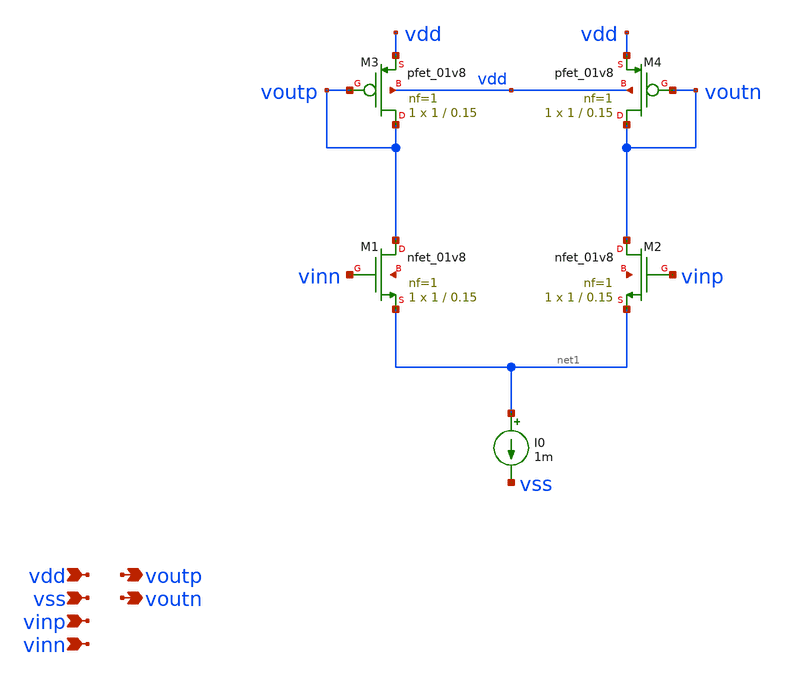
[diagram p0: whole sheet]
** sch_path: schematics/comp_pre_amp.sch
**.subckt comp_pre_amp vdd voutp vss vinp vinn voutn
*.ipin vdd
*.opin voutp
*.ipin vss
*.ipin vinp
*.ipin vinn
*.opin voutn
I0 net1 vss 1m
XM1 voutp vinn net1 net2 sky130_fd_pr__nfet_01v8 L=0.15 W=1 nf=1 ad='int((1 + 1)/2) * 1 / 1 * 0.29' as='int((1 + 2)/2) * 1 / 1 * 0.29'
+ pd='2*int((1 + 1)/2) * (1 / 1 + 0.29)' ps='2*int((1 + 2)/2) * (1 / 1 + 0.29)' nrd='0.29 / 1 ' nrs='0.29 / 1 '
+ sa=0 sb=0 sd=0 mult=1 m=1
XM2 voutn vinp net1 net3 sky130_fd_pr__nfet_01v8 L=0.15 W=1 nf=1 ad='int((1 + 1)/2) * 1 / 1 * 0.29' as='int((1 + 2)/2) * 1 / 1 * 0.29'
+ pd='2*int((1 + 1)/2) * (1 / 1 + 0.29)' ps='2*int((1 + 2)/2) * (1 / 1 + 0.29)' nrd='0.29 / 1 ' nrs='0.29 / 1 '
+ sa=0 sb=0 sd=0 mult=1 m=1
XM3 voutp voutp vdd vdd sky130_fd_pr__pfet_01v8 L=0.15 W=1 nf=1 ad='int((1 + 1)/2) * 1 / 1 * 0.29' as='int((1 + 2)/2) * 1 / 1 * 0.29'
+ pd='2*int((1 + 1)/2) * (1 / 1 + 0.29)' ps='2*int((1 + 2)/2) * (1 / 1 + 0.29)' nrd='0.29 / 1 ' nrs='0.29 / 1 '
+ sa=0 sb=0 sd=0 mult=1 m=1
XM4 voutn voutn vdd vdd sky130_fd_pr__pfet_01v8 L=0.15 W=1 nf=1 ad='int((1 + 1)/2) * 1 / 1 * 0.29' as='int((1 + 2)/2) * 1 / 1 * 0.29'
+ pd='2*int((1 + 1)/2) * (1 / 1 + 0.29)' ps='2*int((1 + 2)/2) * (1 / 1 + 0.29)' nrd='0.29 / 1 ' nrs='0.29 / 1 '
+ sa=0 sb=0 sd=0 mult=1 m=1
**.ends
.end
